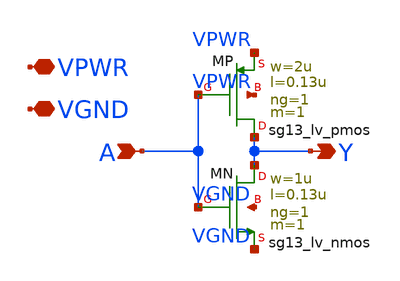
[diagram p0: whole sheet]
** sch_path: xschem/inv_cp.sch
**.subckt inv_cp A Y VPWR VGND
*.ipin A
*.opin Y
*.iopin VPWR
*.iopin VGND
XMP Y A VPWR VPWR sg13_lv_pmos w=2u l=0.13u ng=1 m=1 mm_ok=1
XMN Y A VGND VGND sg13_lv_nmos w=1u l=0.13u ng=1 m=1 mm_ok=1
**.ends
.end
